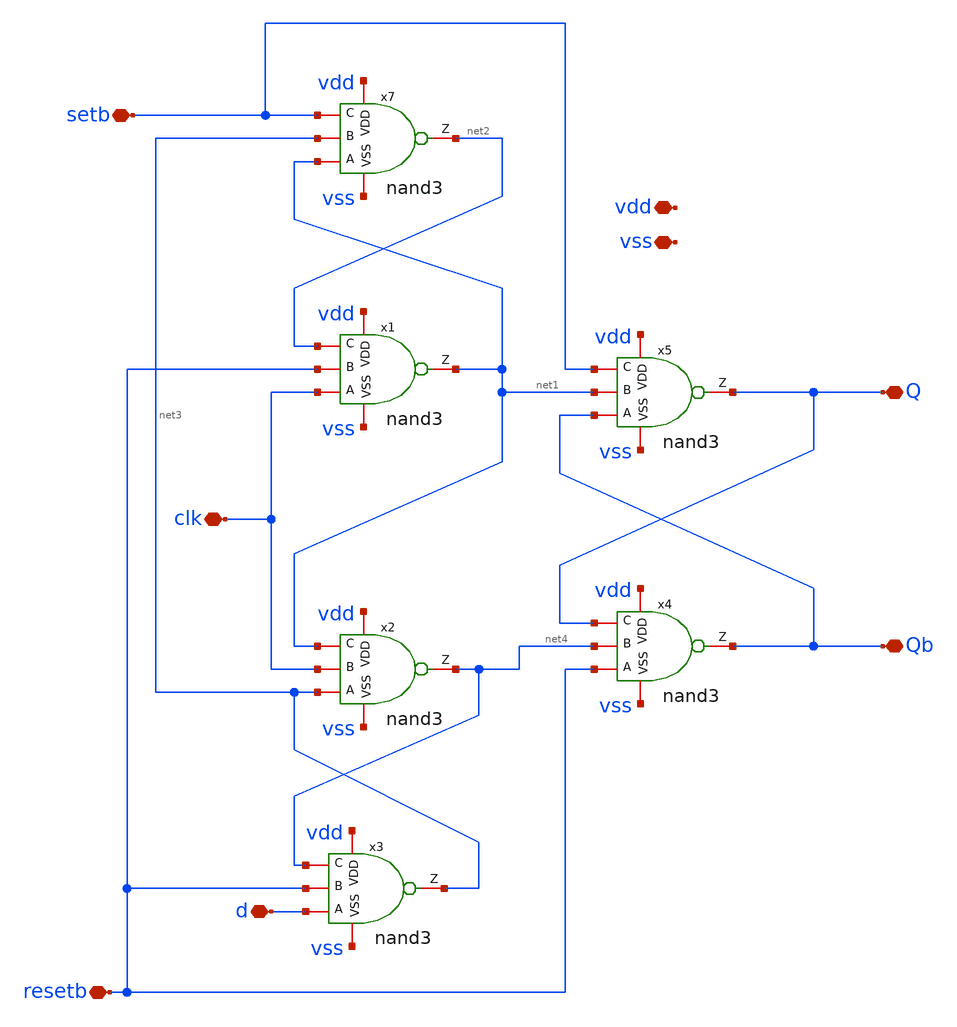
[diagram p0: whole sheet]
** sch_path: Analog/schematics/1_readout/slopedetector/dffrs/dffrs.sch
**.subckt dffrs vdd vss Q Qb d clk resetb setb
*.iopin vdd
*.iopin vss
*.iopin Q
*.iopin Qb
*.iopin d
*.iopin clk
*.iopin resetb
*.iopin setb
x7 vdd net2 net1 net3 setb vss nand3
x1 vdd net1 clk resetb net2 vss nand3
x2 vdd net4 net3 clk net1 vss nand3
x3 vdd net3 d resetb net4 vss nand3
x4 vdd Qb resetb net4 Q vss nand3
x5 vdd Q Qb net1 setb vss nand3
**.ends

* expanding   symbol:  Analog/schematics/1_readout/slopedetector/dffrs/nand3.sym # of pins=6
** sym_path: Analog/schematics/1_readout/slopedetector/dffrs/nand3.sym
** sch_path: Analog/schematics/1_readout/slopedetector/dffrs/nand3.sch
.subckt nand3 VDD Z A B C VSS
*.iopin VDD
*.iopin VSS
*.iopin Z
*.iopin A
*.iopin B
*.iopin C
XM1 Z A net1 VSS nfet_03v3 L=0.4u W=1u nf=1 ad='int((nf+1)/2) * W/nf * 0.18u' as='int((nf+2)/2) * W/nf * 0.18u'
+ pd='2*int((nf+1)/2) * (W/nf + 0.18u)' ps='2*int((nf+2)/2) * (W/nf + 0.18u)' nrd='0.18u / W' nrs='0.18u / W'
+ sa=0 sb=0 sd=0 m=1
XM2 net1 B net2 VSS nfet_03v3 L=0.4u W=1u nf=1 ad='int((nf+1)/2) * W/nf * 0.18u' as='int((nf+2)/2) * W/nf * 0.18u'
+ pd='2*int((nf+1)/2) * (W/nf + 0.18u)' ps='2*int((nf+2)/2) * (W/nf + 0.18u)' nrd='0.18u / W' nrs='0.18u / W'
+ sa=0 sb=0 sd=0 m=1
XM3 Z B VDD VDD pfet_03v3 L=0.4u W=2.5u nf=1 ad='int((nf+1)/2) * W/nf * 0.18u' as='int((nf+2)/2) * W/nf * 0.18u'
+ pd='2*int((nf+1)/2) * (W/nf + 0.18u)' ps='2*int((nf+2)/2) * (W/nf + 0.18u)' nrd='0.18u / W' nrs='0.18u / W'
+ sa=0 sb=0 sd=0 m=1
XM4 Z A VDD VDD pfet_03v3 L=0.4u W=2.5u nf=1 ad='int((nf+1)/2) * W/nf * 0.18u' as='int((nf+2)/2) * W/nf * 0.18u'
+ pd='2*int((nf+1)/2) * (W/nf + 0.18u)' ps='2*int((nf+2)/2) * (W/nf + 0.18u)' nrd='0.18u / W' nrs='0.18u / W'
+ sa=0 sb=0 sd=0 m=1
XM5 Z C VDD VDD pfet_03v3 L=0.4u W=2.5u nf=1 ad='int((nf+1)/2) * W/nf * 0.18u' as='int((nf+2)/2) * W/nf * 0.18u'
+ pd='2*int((nf+1)/2) * (W/nf + 0.18u)' ps='2*int((nf+2)/2) * (W/nf + 0.18u)' nrd='0.18u / W' nrs='0.18u / W'
+ sa=0 sb=0 sd=0 m=1
XM6 net2 C VSS VSS nfet_03v3 L=0.4u W=1u nf=1 ad='int((nf+1)/2) * W/nf * 0.18u' as='int((nf+2)/2) * W/nf * 0.18u'
+ pd='2*int((nf+1)/2) * (W/nf + 0.18u)' ps='2*int((nf+2)/2) * (W/nf + 0.18u)' nrd='0.18u / W' nrs='0.18u / W'
+ sa=0 sb=0 sd=0 m=1
.ends

.end
